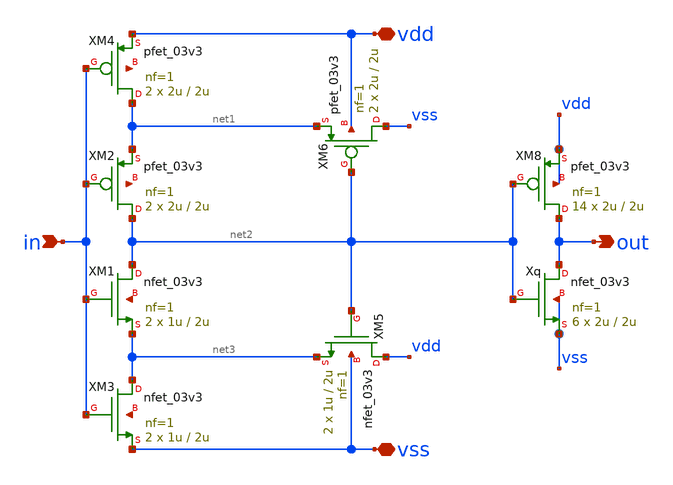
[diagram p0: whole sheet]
** sch_path: design/analog/schmitt_trigger/schmitt_trigger_v2.sch
**.subckt schmitt_trigger_v2 in out vdd vss
*.ipin in
*.opin out
*.iopin vdd
*.iopin vss
XM1 net2 in net3 net4 nfet_03v3 L=2u W=1u nf=1 ad='int((nf+1)/2) * W/nf * 0.18u' as='int((nf+2)/2) * W/nf * 0.18u'
+ pd='2*int((nf+1)/2) * (W/nf + 0.18u)' ps='2*int((nf+2)/2) * (W/nf + 0.18u)' nrd='0.18u / W' nrs='0.18u / W'
+ sa=0 sb=0 sd=0 m=2
XM2 net2 in net1 net5 pfet_03v3 L=2u W=2u nf=1 ad='int((nf+1)/2) * W/nf * 0.18u' as='int((nf+2)/2) * W/nf * 0.18u'
+ pd='2*int((nf+1)/2) * (W/nf + 0.18u)' ps='2*int((nf+2)/2) * (W/nf + 0.18u)' nrd='0.18u / W' nrs='0.18u / W'
+ sa=0 sb=0 sd=0 m=2
XM3 net3 in vss net6 nfet_03v3 L=2u W=1u nf=1 ad='int((nf+1)/2) * W/nf * 0.18u' as='int((nf+2)/2) * W/nf * 0.18u'
+ pd='2*int((nf+1)/2) * (W/nf + 0.18u)' ps='2*int((nf+2)/2) * (W/nf + 0.18u)' nrd='0.18u / W' nrs='0.18u / W'
+ sa=0 sb=0 sd=0 m=2
XM4 net1 in vdd net7 pfet_03v3 L=2u W=2u nf=1 ad='int((nf+1)/2) * W/nf * 0.18u' as='int((nf+2)/2) * W/nf * 0.18u'
+ pd='2*int((nf+1)/2) * (W/nf + 0.18u)' ps='2*int((nf+2)/2) * (W/nf + 0.18u)' nrd='0.18u / W' nrs='0.18u / W'
+ sa=0 sb=0 sd=0 m=2
XM5 vdd net2 net3 vss nfet_03v3 L=2u W=1u nf=1 ad='int((nf+1)/2) * W/nf * 0.18u' as='int((nf+2)/2) * W/nf * 0.18u'
+ pd='2*int((nf+1)/2) * (W/nf + 0.18u)' ps='2*int((nf+2)/2) * (W/nf + 0.18u)' nrd='0.18u / W' nrs='0.18u / W'
+ sa=0 sb=0 sd=0 m=2
XM6 vss net2 net1 vdd pfet_03v3 L=2u W=2u nf=1 ad='int((nf+1)/2) * W/nf * 0.18u' as='int((nf+2)/2) * W/nf * 0.18u'
+ pd='2*int((nf+1)/2) * (W/nf + 0.18u)' ps='2*int((nf+2)/2) * (W/nf + 0.18u)' nrd='0.18u / W' nrs='0.18u / W'
+ sa=0 sb=0 sd=0 m=2
Xq out net2 vss vss nfet_03v3 L=2u W=2u nf=1 ad='int((nf+1)/2) * W/nf * 0.18u' as='int((nf+2)/2) * W/nf * 0.18u'
+ pd='2*int((nf+1)/2) * (W/nf + 0.18u)' ps='2*int((nf+2)/2) * (W/nf + 0.18u)' nrd='0.18u / W' nrs='0.18u / W'
+ sa=0 sb=0 sd=0 m=6
XM8 out net2 vdd vdd pfet_03v3 L=2u W=2u nf=1 ad='int((nf+1)/2) * W/nf * 0.18u' as='int((nf+2)/2) * W/nf * 0.18u'
+ pd='2*int((nf+1)/2) * (W/nf + 0.18u)' ps='2*int((nf+2)/2) * (W/nf + 0.18u)' nrd='0.18u / W' nrs='0.18u / W'
+ sa=0 sb=0 sd=0 m=14
**.ends
.end
